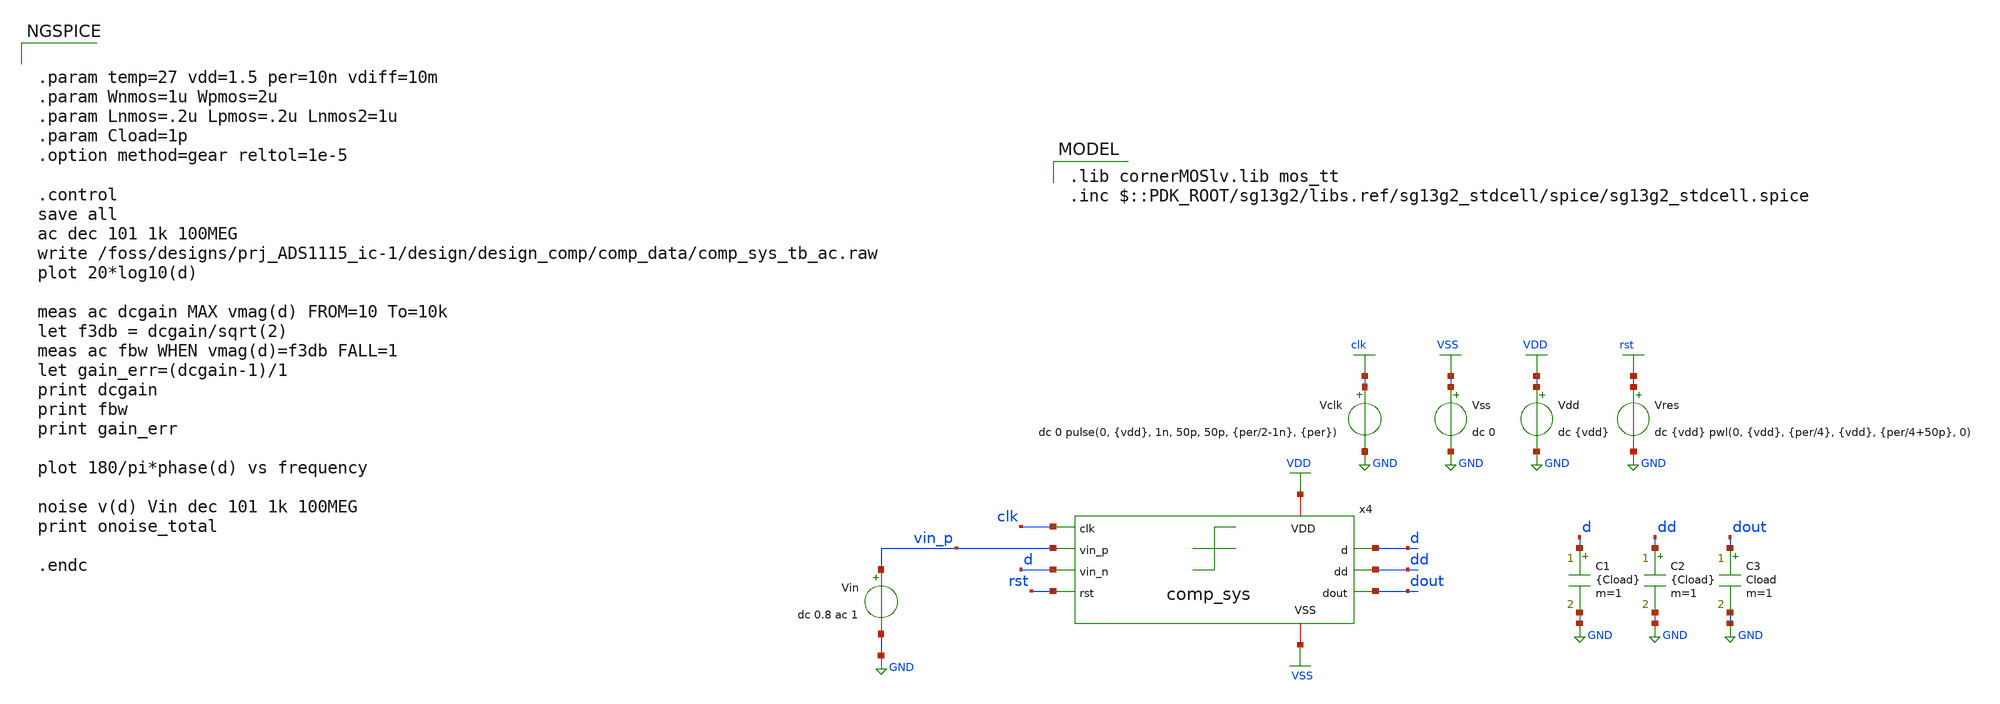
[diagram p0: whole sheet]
** sch_path: design/design_comp/tb_comp_sys_ac.sch
**.subckt tb_comp_sys_ac
Vdd VDD GND dc {vdd}
Vss VSS GND dc 0
Vin vin_p GND dc 0.8 ac 1
Vclk clk GND dc 0 pulse(0, {vdd}, 1n, 50p, 50p, {per/2-1n}, {per})
Vres rst GND dc {vdd} pwl(0, {vdd}, {per/4}, {vdd}, {per/4+50p}, 0)
x4 VDD clk d vin_p d dd rst dout VSS comp_sys
C1 d GND {Cload} m=1
C2 dd GND {Cload} m=1
C3 dout GND Cload m=1
**** begin user architecture code


.param temp=27 vdd=1.5 per=10n vdiff=10m
.param Wnmos=1u Wpmos=2u
.param Lnmos=.2u Lpmos=.2u Lnmos2=1u
.param Cload=1p
.option method=gear reltol=1e-5

.control
save all
ac dec 101 1k 100MEG
write /foss/designs/prj_ADS1115_ic-1/design/design_comp/comp_data/comp_sys_tb_ac.raw
plot 20*log10(d)

meas ac dcgain MAX vmag(d) FROM=10 To=10k
let f3db = dcgain/sqrt(2)
meas ac fbw WHEN vmag(d)=f3db FALL=1
let gain_err=(dcgain-1)/1
print dcgain
print fbw
print gain_err

plot 180/pi*phase(d) vs frequency

noise v(d) Vin dec 101 1k 100MEG
print onoise_total

.endc

 .lib cornerMOSlv.lib mos_tt
.inc $::PDK_ROOT/sg13g2/libs.ref/sg13g2_stdcell/spice/sg13g2_stdcell.spice
**** end user architecture code
**.ends
.GLOBAL GND
.GLOBAL VDD
.GLOBAL VSS
.GLOBAL clk
.GLOBAL rst
.end
